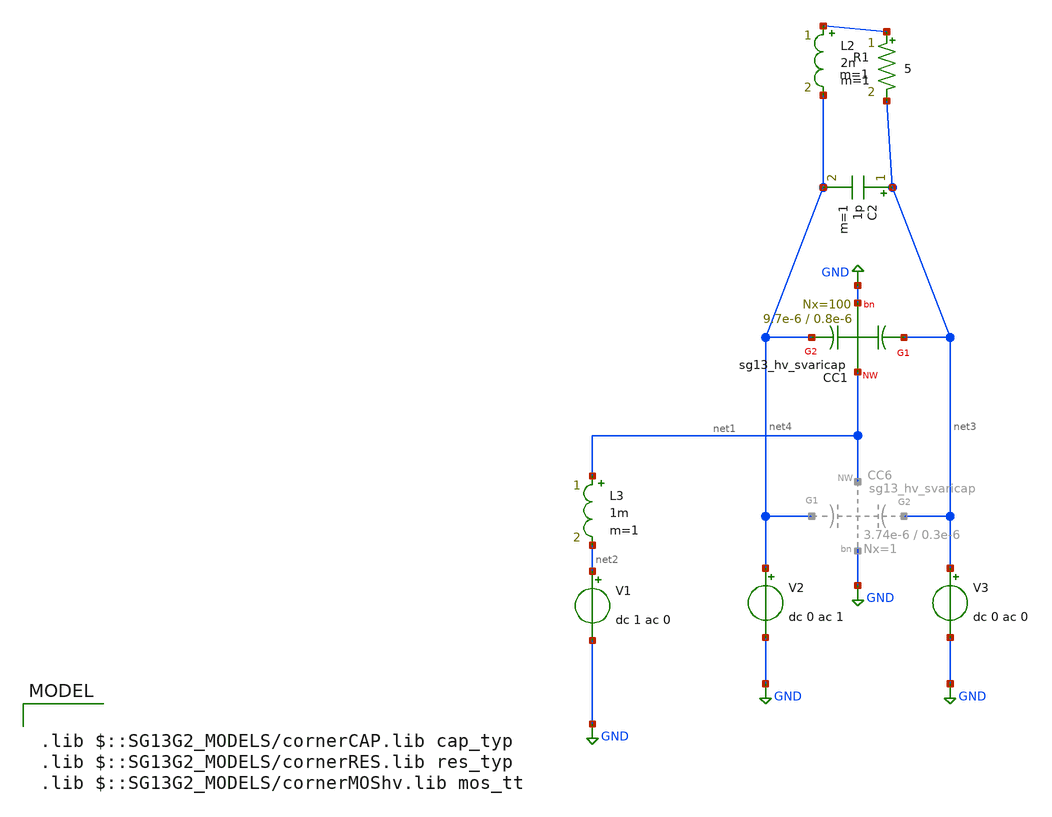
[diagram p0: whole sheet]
** sch_path: design_data/xschem/measuremenst_and_test_of_idas/ac_svaricap_test5.sch
**.subckt ac_svaricap_test5
V1 net2 GND dc 1 ac 0
L3 net1 net2 1m m=1
V3 net3 GND dc 0 ac 0
V2 net4 GND dc 0 ac 1
XC1 net3 net1 net4 GND sg13_hv_svaricap w=9.7e-6 l=0.8e-6 Nx=100
C2 net3 net4 1p m=1
R1 net5 net3 5 m=1
L2 net5 net4 2n m=1
**** begin user architecture code

.lib $::SG13G2_MODELS/cornerCAP.lib cap_typ
.lib $::SG13G2_MODELS/cornerRES.lib res_typ
.lib $::SG13G2_MODELS/cornerMOShv.lib mos_tt



*.param temp=27
.control
save all


op
write ac_mosvar.raw
set appendwrite

let vfreq = 0
while vfreq < 1.8
   alter v1 = vfreq
   ac lin 1000 .1GHz 10GHz
   let I1=(i(V3))
   let Ctot=imag(I1)/(2*3.1415*frequency)
   let Q=imag(I1)/real(I1)
   write ac_mosvar.raw
   set appendwrite

   let vfreq = vfreq + 0.1
end

   alter v1 = 1.8
   ac lin 1000 .1GHz 10GHz
   let I1=(i(V3))
   let Ctot=imag(I1)/(2*3.1415*frequency)
   let Q=imag(I1)/real(I1)
   write ac_mosvar.raw
   set appendwrite

   alter c2 = 300f
   ac lin 1000 .1GHz 10GHz
   let I1=(i(V3))
   let Ctot=imag(I1)/(2*3.1415*frequency)
   let Q=imag(I1)/real(I1)
   write ac_mosvar.raw
   set appendwrite

   alter c2 = 100f
   ac lin 1000 .1GHz 10GHz
   let I1=(i(V3))
   let Ctot=imag(I1)/(2*3.1415*frequency)
   let Q=imag(I1)/real(I1)
   write ac_mosvar.raw
   set appendwrite

   alter c2 = 30f
   ac lin 1000 .1GHz 10GHz
   let I1=(i(V3))
   let Ctot=imag(I1)/(2*3.1415*frequency)
   let Q=imag(I1)/real(I1)
   write ac_mosvar.raw
   set appendwrite

   alter c2 = 1f
   ac lin 1000 .1GHz 10GHz
   let I1=(i(V3))
   let Ctot=imag(I1)/(2*3.1415*frequency)
   let Q=imag(I1)/real(I1)
   write ac_mosvar.raw
   set appendwrite

   alter c1 nx = 30
   ac lin 1000 .1GHz 10GHz
   let I1=(i(V3))
   let Ctot=imag(I1)/(2*3.1415*frequency)
   let Q=imag(I1)/real(I1)
   write ac_mosvar.raw
   set appendwrite


*plot i(v1)

.endc


**** end user architecture code
**.ends
.GLOBAL GND
.end
